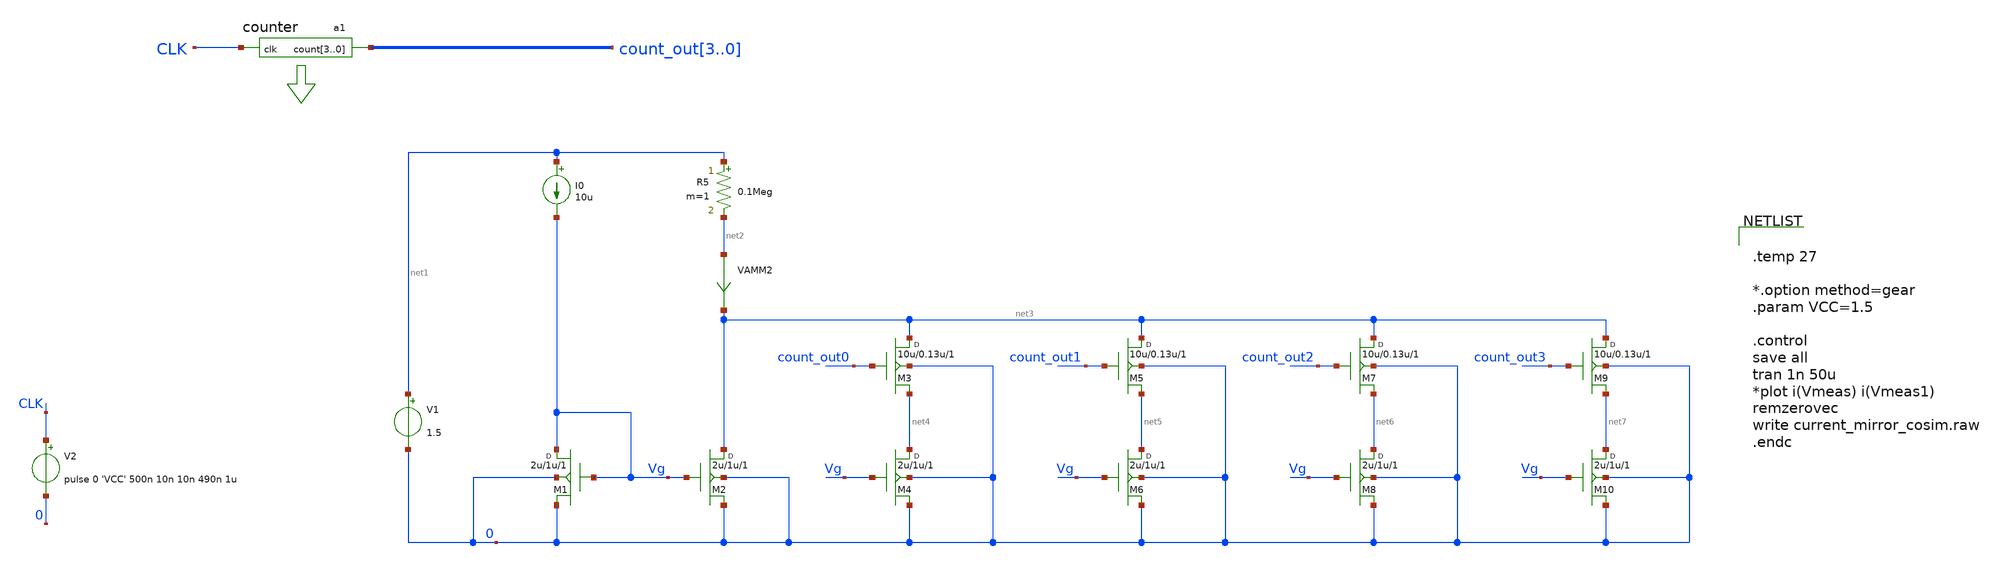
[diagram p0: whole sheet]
** sch_path: xschem/current_mirror_cosim.sch
**.subckt current_mirror_cosim
a1 [ CLK ] [ count_out3 count_out2 count_out1 count_out0 ] counter
V2 CLK 0 pulse 0 'VCC' 500n 10n 10n 490n 1u
M1 Vg Vg 0 0 nm w=2u l=1u m=1
I0 net1 Vg 10u
V1 net1 0 1.5
M2 net3 Vg 0 0 nm w=2u l=1u m=1
R5 net1 net2 0.1Meg m=1
VAMM2 net2 net3 0
M3 net3 count_out0 net4 0 nm w=10u l=0.13u m=1
M4 net4 Vg 0 0 nm w=2u l=1u m=1
M5 net3 count_out1 net5 0 nm w=10u l=0.13u m=1
M6 net5 Vg 0 0 nm w=2u l=1u m=1
M7 net3 count_out2 net6 0 nm w=10u l=0.13u m=1
M8 net6 Vg 0 0 nm w=2u l=1u m=1
M9 net3 count_out3 net7 0 nm w=10u l=0.13u m=1
M10 net7 Vg 0 0 nm w=2u l=1u m=1
**** begin user architecture code


.temp 27

*.option method=gear
.param VCC=1.5

.control
save all
tran 1n 50u
*plot i(Vmeas) i(Vmeas1)
remzerovec
write current_mirror_cosim.raw
.endc


**** end user architecture code
**.ends
**** begin user architecture code
.model nm nmos level=54 version=4.8.3
.model counter d_cosim simulation="ivlng" sim_args=["counter"] delay=0
**** end user architecture code
.end
